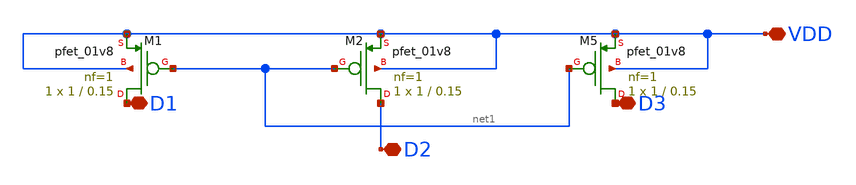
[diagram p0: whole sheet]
** sch_path: opamp/mag/nmoscs/pmos.sch
**.subckt pmos VDD D2 D1 D3
*.iopin VDD
*.iopin D2
*.iopin D1
*.iopin D3
XM1 D1 net1 VDD VDD sky130_fd_pr__pfet_01v8 L=0.15 W=1 nf=1 ad='int((nf+1)/2) * W/nf * 0.29' as='int((nf+2)/2) * W/nf * 0.29'
+ pd='2*int((nf+1)/2) * (W/nf + 0.29)' ps='2*int((nf+2)/2) * (W/nf + 0.29)' nrd='0.29 / W' nrs='0.29 / W'
+ sa=0 sb=0 sd=0 mult=1 m=1
XM2 D2 net1 VDD VDD sky130_fd_pr__pfet_01v8 L=0.15 W=1 nf=1 ad='int((nf+1)/2) * W/nf * 0.29' as='int((nf+2)/2) * W/nf * 0.29'
+ pd='2*int((nf+1)/2) * (W/nf + 0.29)' ps='2*int((nf+2)/2) * (W/nf + 0.29)' nrd='0.29 / W' nrs='0.29 / W'
+ sa=0 sb=0 sd=0 mult=1 m=1
XM5 D3 net1 VDD VDD sky130_fd_pr__pfet_01v8 L=0.15 W=1 nf=1 ad='int((nf+1)/2) * W/nf * 0.29' as='int((nf+2)/2) * W/nf * 0.29'
+ pd='2*int((nf+1)/2) * (W/nf + 0.29)' ps='2*int((nf+2)/2) * (W/nf + 0.29)' nrd='0.29 / W' nrs='0.29 / W'
+ sa=0 sb=0 sd=0 mult=1 m=1
**.ends
.end
